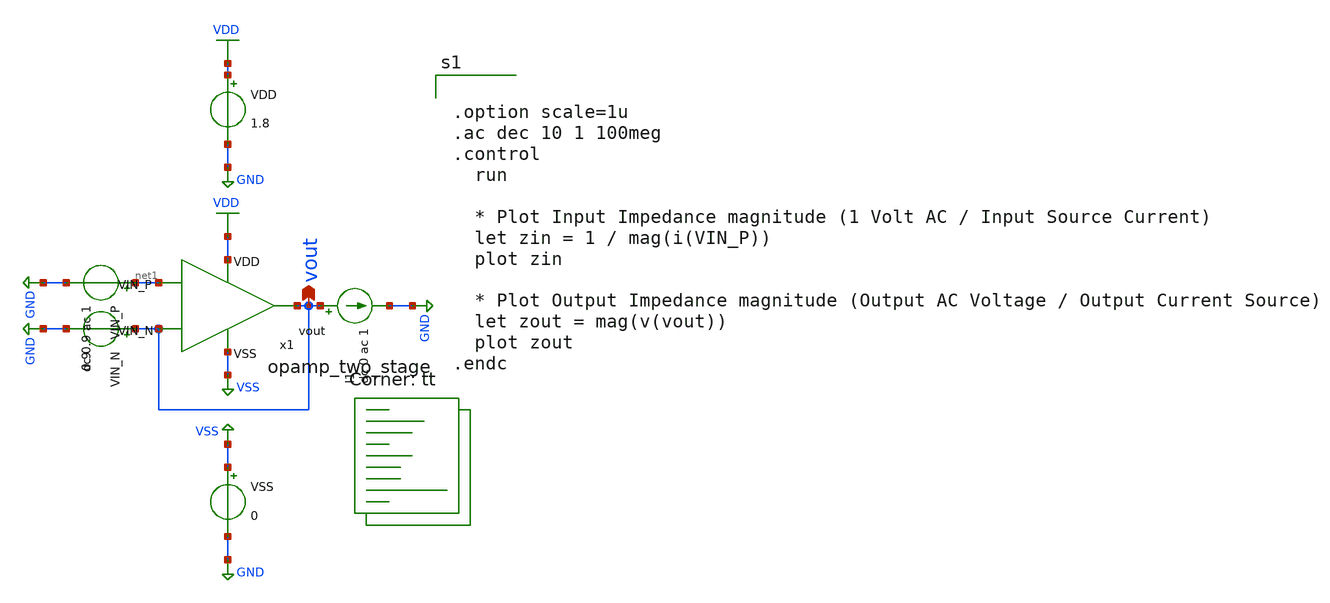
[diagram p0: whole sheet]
** sch_path: analog/schematics/tb_impedance.sch
**.subckt tb_impedance vout
*.opin vout
VDD VDD GND 1.8
VSS VSS GND 0
x1 VDD vout net1 vout VSS opamp_two_stage
VIN_N vout GND 0.9
I1 vout GND dc 0 ac 1
VIN_P net1 GND dc 0.9 ac 1
**** begin user architecture code


.option scale=1u
.ac dec 10 1 100meg
.control
  run

  * Plot Input Impedance magnitude (1 Volt AC / Input Source Current)
  let zin = 1 / mag(i(VIN_P))
  plot zin

  * Plot Output Impedance magnitude (Output AC Voltage / Output Current Source)
  let zout = mag(v(vout))
  plot zout
.endc


.lib $::SKYWATER_MODELS/sky130.lib.spice tt
**** end user architecture code
**.ends

* expanding   symbol:  opamp_two_stage.sym # of pins=5
** sym_path: analog/schematics/opamp_two_stage.sym
** sch_path: analog/schematics/opamp_two_stage.sch
.subckt opamp_two_stage VDD vout VIN_P VIN_N VSS
*.ipin VIN_P
*.ipin VIN_N
*.opin vout
*.ipin VDD
*.ipin VSS
XM1 net3 VIN_N net4 VSS sky130_fd_pr__nfet_01v8 L=0.3 W=2 nf=1 ad='int((nf+1)/2) * W/nf * 0.29' as='int((nf+2)/2) * W/nf * 0.29'
+ pd='2*int((nf+1)/2) * (W/nf + 0.29)' ps='2*int((nf+2)/2) * (W/nf + 0.29)' nrd='0.29 / W' nrs='0.29 / W'
+ sa=0 sb=0 sd=0 mult=1 m=1
XM2 net5 VIN_P net4 VSS sky130_fd_pr__nfet_01v8 L=0.3 W=2 nf=1 ad='int((nf+1)/2) * W/nf * 0.29' as='int((nf+2)/2) * W/nf * 0.29'
+ pd='2*int((nf+1)/2) * (W/nf + 0.29)' ps='2*int((nf+2)/2) * (W/nf + 0.29)' nrd='0.29 / W' nrs='0.29 / W'
+ sa=0 sb=0 sd=0 mult=1 m=1
XM3 net3 net5 VDD VDD sky130_fd_pr__pfet_01v8 L=0.3 W=2 nf=1 ad='int((nf+1)/2) * W/nf * 0.29' as='int((nf+2)/2) * W/nf * 0.29'
+ pd='2*int((nf+1)/2) * (W/nf + 0.29)' ps='2*int((nf+2)/2) * (W/nf + 0.29)' nrd='0.29 / W' nrs='0.29 / W'
+ sa=0 sb=0 sd=0 mult=1 m=1
XM4 net5 net5 VDD VDD sky130_fd_pr__pfet_01v8 L=0.3 W=2 nf=1 ad='int((nf+1)/2) * W/nf * 0.29' as='int((nf+2)/2) * W/nf * 0.29'
+ pd='2*int((nf+1)/2) * (W/nf + 0.29)' ps='2*int((nf+2)/2) * (W/nf + 0.29)' nrd='0.29 / W' nrs='0.29 / W'
+ sa=0 sb=0 sd=0 mult=1 m=1
XM5 vout net3 VDD VDD sky130_fd_pr__pfet_01v8 L=0.3 W=2 nf=1 ad='int((nf+1)/2) * W/nf * 0.29' as='int((nf+2)/2) * W/nf * 0.29'
+ pd='2*int((nf+1)/2) * (W/nf + 0.29)' ps='2*int((nf+2)/2) * (W/nf + 0.29)' nrd='0.29 / W' nrs='0.29 / W'
+ sa=0 sb=0 sd=0 mult=2 m=2
XM6 vout net1 VSS VSS sky130_fd_pr__nfet_01v8 L=1 W=2 nf=1 ad='int((nf+1)/2) * W/nf * 0.29' as='int((nf+2)/2) * W/nf * 0.29'
+ pd='2*int((nf+1)/2) * (W/nf + 0.29)' ps='2*int((nf+2)/2) * (W/nf + 0.29)' nrd='0.29 / W' nrs='0.29 / W'
+ sa=0 sb=0 sd=0 mult=2 m=2
XM7 net4 net1 VSS VSS sky130_fd_pr__nfet_01v8 L=1 W=2 nf=1 ad='int((nf+1)/2) * W/nf * 0.29' as='int((nf+2)/2) * W/nf * 0.29'
+ pd='2*int((nf+1)/2) * (W/nf + 0.29)' ps='2*int((nf+2)/2) * (W/nf + 0.29)' nrd='0.29 / W' nrs='0.29 / W'
+ sa=0 sb=0 sd=0 mult=2 m=2
XR1 net3 net2 VSS sky130_fd_pr__res_high_po W=1 L=1 mult=1 m=1
XC1 vout net2 sky130_fd_pr__cap_mim_m3_1 W=1 L=1 MF=1 m=1
XR2 net1 VDD VSS sky130_fd_pr__res_high_po W=1 L=1 mult=1 m=1
XR3 VSS net1 VSS sky130_fd_pr__res_high_po W=1 L=1 mult=1 m=1
.ends

.GLOBAL VDD
.GLOBAL GND
.GLOBAL VSS
.end
